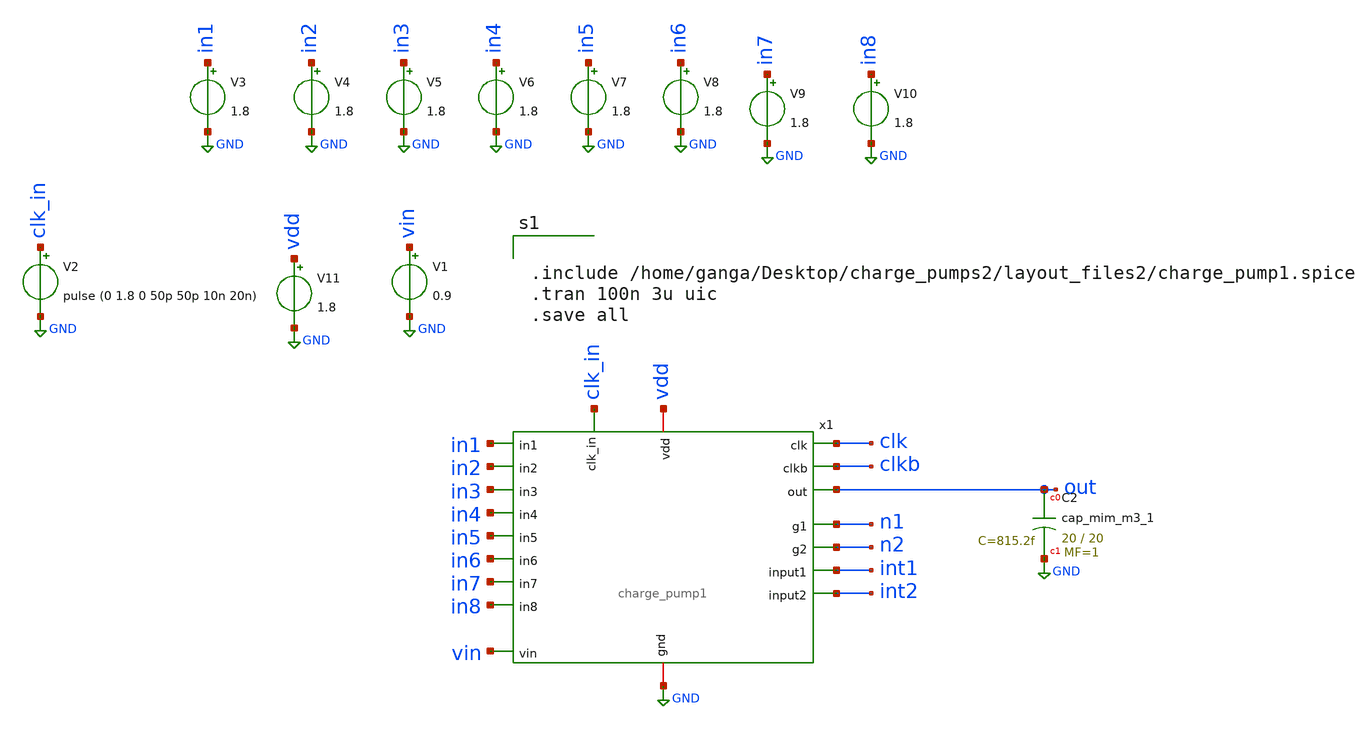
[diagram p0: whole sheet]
** sch_path: xschem/charge_pumps2/CP1_post_layout.sch
**.subckt CP1_post_layout
V1 vin GND 0.9
V2 clk_in GND pulse (0 1.8 0 50p 50p 10n 20n)
V3 in1 GND 1.8
V4 in2 GND 1.8
V5 in3 GND 1.8
V6 in4 GND 1.8
V7 in5 GND 1.8
V8 in6 GND 1.8
V9 in7 GND 1.8
V10 in8 GND 1.8
V11 vdd GND 1.8
XC2 out GND sky130_fd_pr__cap_mim_m3_1 W=20 L=20 MF=1 m=1
x1 clk_in int1 int2 vdd GND in1 in3 in2 in4 in5 in6 in7 in8 vin n1 n2 clk clkb charge_pump1
**** begin user architecture code

** opencircuitdesign pdks install
.lib $::SKYWATER_MODELS/sky130.lib.spice tt




.include /home/ganga/Desktop/charge_pumps2/layout_files2/charge_pump1.spice
.tran 100n 3u uic
.save all


**** end user architecture code
**.ends
.GLOBAL GND
.end
